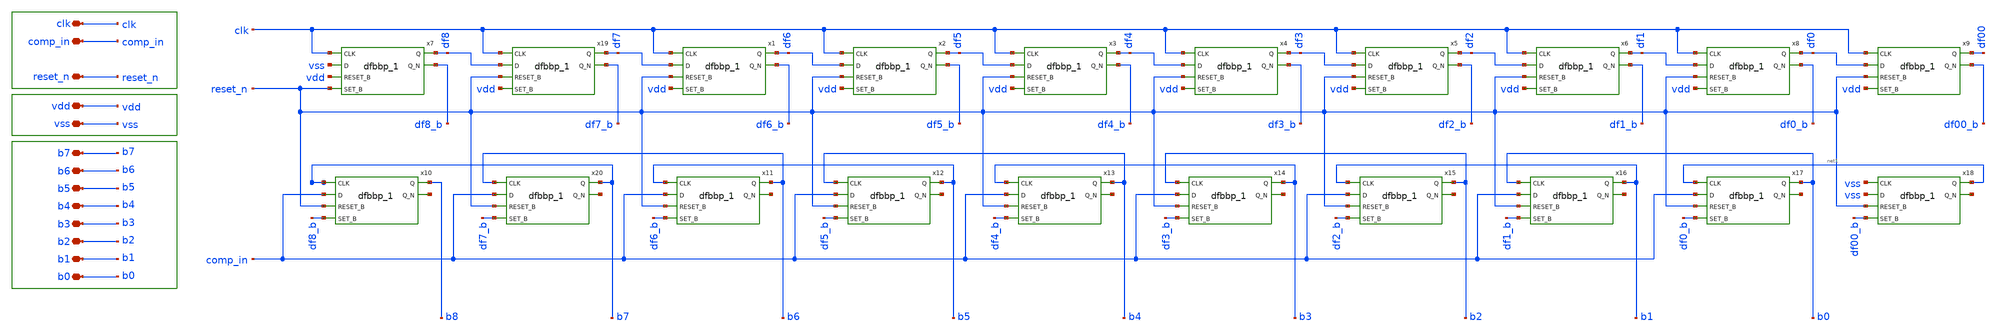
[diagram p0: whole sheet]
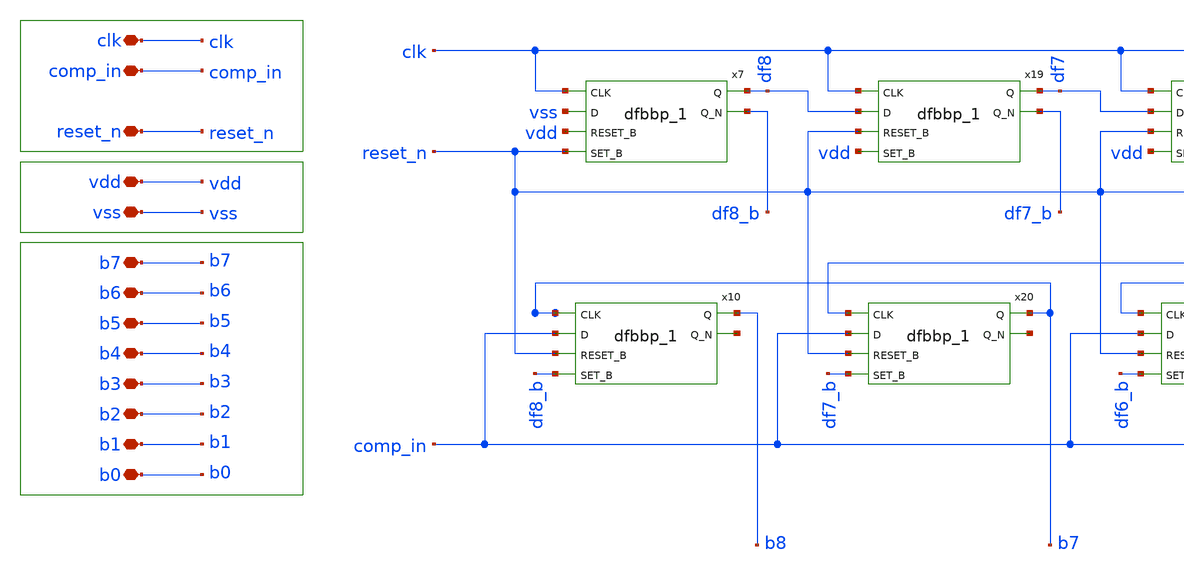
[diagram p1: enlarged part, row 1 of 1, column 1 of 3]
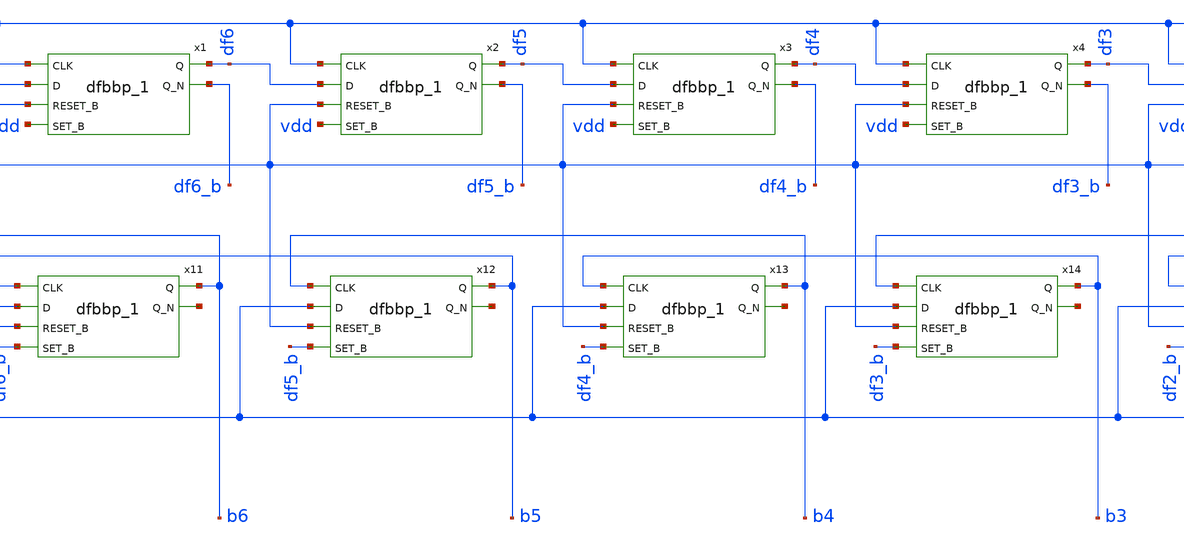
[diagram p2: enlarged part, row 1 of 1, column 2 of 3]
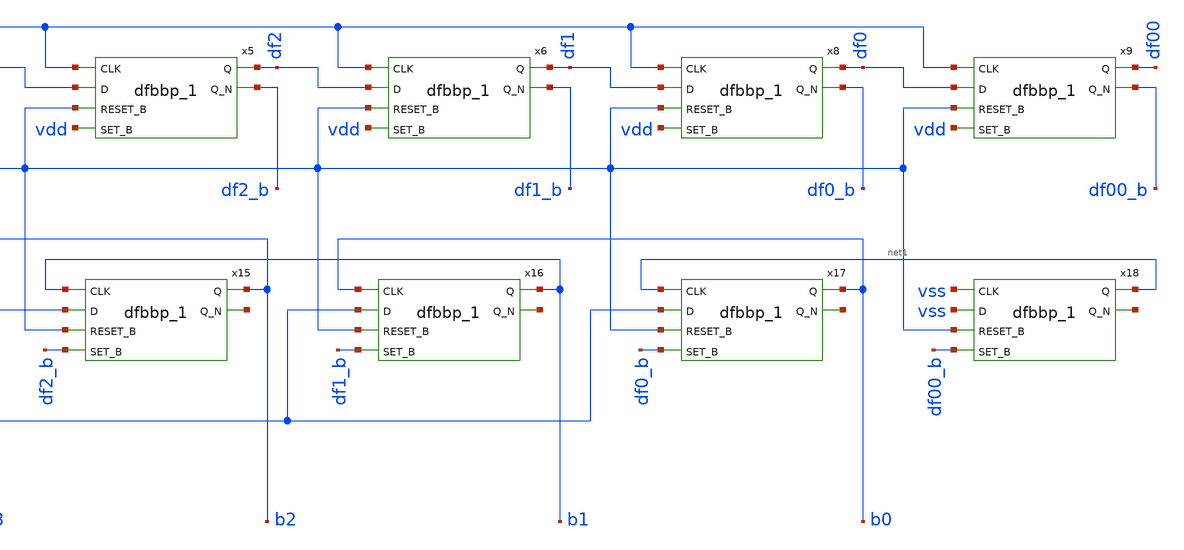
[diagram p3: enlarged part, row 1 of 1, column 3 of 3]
** sch_path: xschem/sar_logic/sarlogic.sch
**.subckt sarlogic vdd clk b7 b6 b5 b4 b3 b2 b1 b0 comp_in vss reset_n
*.iopin vdd
*.iopin clk
*.iopin b7
*.iopin b6
*.iopin b5
*.iopin b4
*.iopin b3
*.iopin b2
*.iopin b1
*.iopin b0
*.iopin comp_in
*.iopin vss
*.iopin reset_n
x7 clk vss vdd reset_n vss vss vdd vdd df8 df8_b sky130_fd_sc_hd__dfbbp_1
x1 clk df7 reset_n vdd vss vss vdd vdd df6 df6_b sky130_fd_sc_hd__dfbbp_1
x2 clk df6 reset_n vdd vss vss vdd vdd df5 df5_b sky130_fd_sc_hd__dfbbp_1
x3 clk df5 reset_n vdd vss vss vdd vdd df4 df4_b sky130_fd_sc_hd__dfbbp_1
x4 clk df4 reset_n vdd vss vss vdd vdd df3 df3_b sky130_fd_sc_hd__dfbbp_1
x5 clk df3 reset_n vdd vss vss vdd vdd df2 df2_b sky130_fd_sc_hd__dfbbp_1
x6 clk df2 reset_n vdd vss vss vdd vdd df1 df1_b sky130_fd_sc_hd__dfbbp_1
x8 clk df1 reset_n vdd vss vss vdd vdd df0 df0_b sky130_fd_sc_hd__dfbbp_1
x9 clk df0 reset_n vdd vss vss vdd vdd df00 df00_b sky130_fd_sc_hd__dfbbp_1
x10 b7 comp_in reset_n df8_b vss vss vdd vdd b8 net2 sky130_fd_sc_hd__dfbbp_1
x11 b5 comp_in reset_n df6_b vss vss vdd vdd b6 net3 sky130_fd_sc_hd__dfbbp_1
x12 b4 comp_in reset_n df5_b vss vss vdd vdd b5 net4 sky130_fd_sc_hd__dfbbp_1
x13 b3 comp_in reset_n df4_b vss vss vdd vdd b4 net5 sky130_fd_sc_hd__dfbbp_1
x14 b2 comp_in reset_n df3_b vss vss vdd vdd b3 net6 sky130_fd_sc_hd__dfbbp_1
x15 b1 comp_in reset_n df2_b vss vss vdd vdd b2 net7 sky130_fd_sc_hd__dfbbp_1
x16 b0 comp_in reset_n df1_b vss vss vdd vdd b1 net8 sky130_fd_sc_hd__dfbbp_1
x17 net1 comp_in reset_n df0_b vss vss vdd vdd b0 net9 sky130_fd_sc_hd__dfbbp_1
x18 vss vss reset_n df00_b vss vss vdd vdd net1 net10 sky130_fd_sc_hd__dfbbp_1
x19 clk df8 reset_n vdd vss vss vdd vdd df7 df7_b sky130_fd_sc_hd__dfbbp_1
x20 b6 comp_in reset_n df7_b vss vss vdd vdd b7 net11 sky130_fd_sc_hd__dfbbp_1
**.ends
.end
